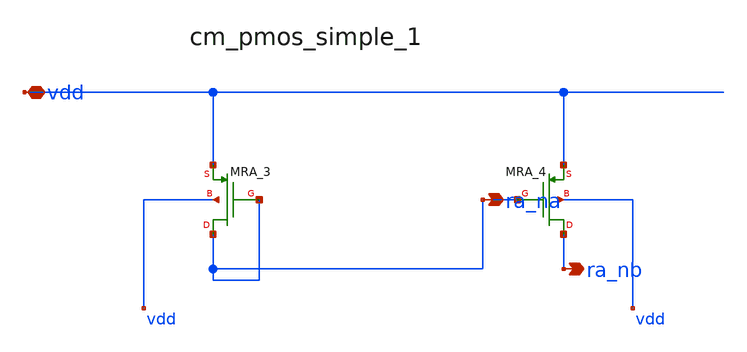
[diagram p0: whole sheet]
** sch_path: analog-db/raw/ldo_005_buffered_ref/hier/blocks/cm_pmos_simple_1.sch
**.subckt cm_pmos_simple_1 vdd ra_na ra_nb
*.iopin vdd
*.opin ra_na
*.opin ra_nb
XMRA_3 ra_na ra_na vdd vdd sg13_hv_pmos w=x_dut_xmra_3_w l=x_dut_xmra_3_l ng=1 m=1
XMRA_4 ra_nb ra_na vdd vdd sg13_hv_pmos w=x_dut_xmra_4_w l=x_dut_xmra_4_l ng=1 m=1
**.ends
.end
